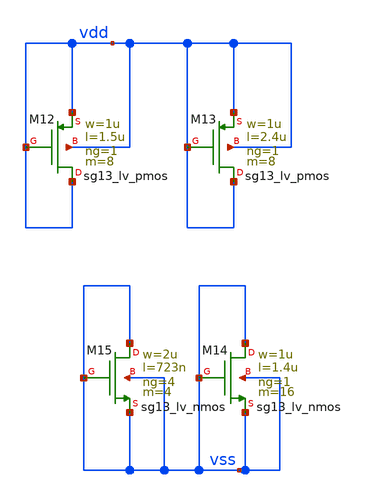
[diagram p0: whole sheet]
** sch_path: v2_feature_extr_withf/ota_p_wr_dummy_dev.sch
**.subckt ota_p_wr_dummy_dev
XM12 vdd vdd vdd vdd sg13_lv_pmos w=1u l=1.5u ng=1 m=8 mm_ok=1
XM13 vdd vdd vdd vdd sg13_lv_pmos w=1u l=2.4u ng=1 m=8 mm_ok=1
XM14 vss vss vss vss sg13_lv_nmos w=1u l=1.4u ng=1 m=16 mm_ok=1
XM15 vss vss vss vss sg13_lv_nmos w=2u l=723n ng=4 m=4 mm_ok=1
**.ends
.end
